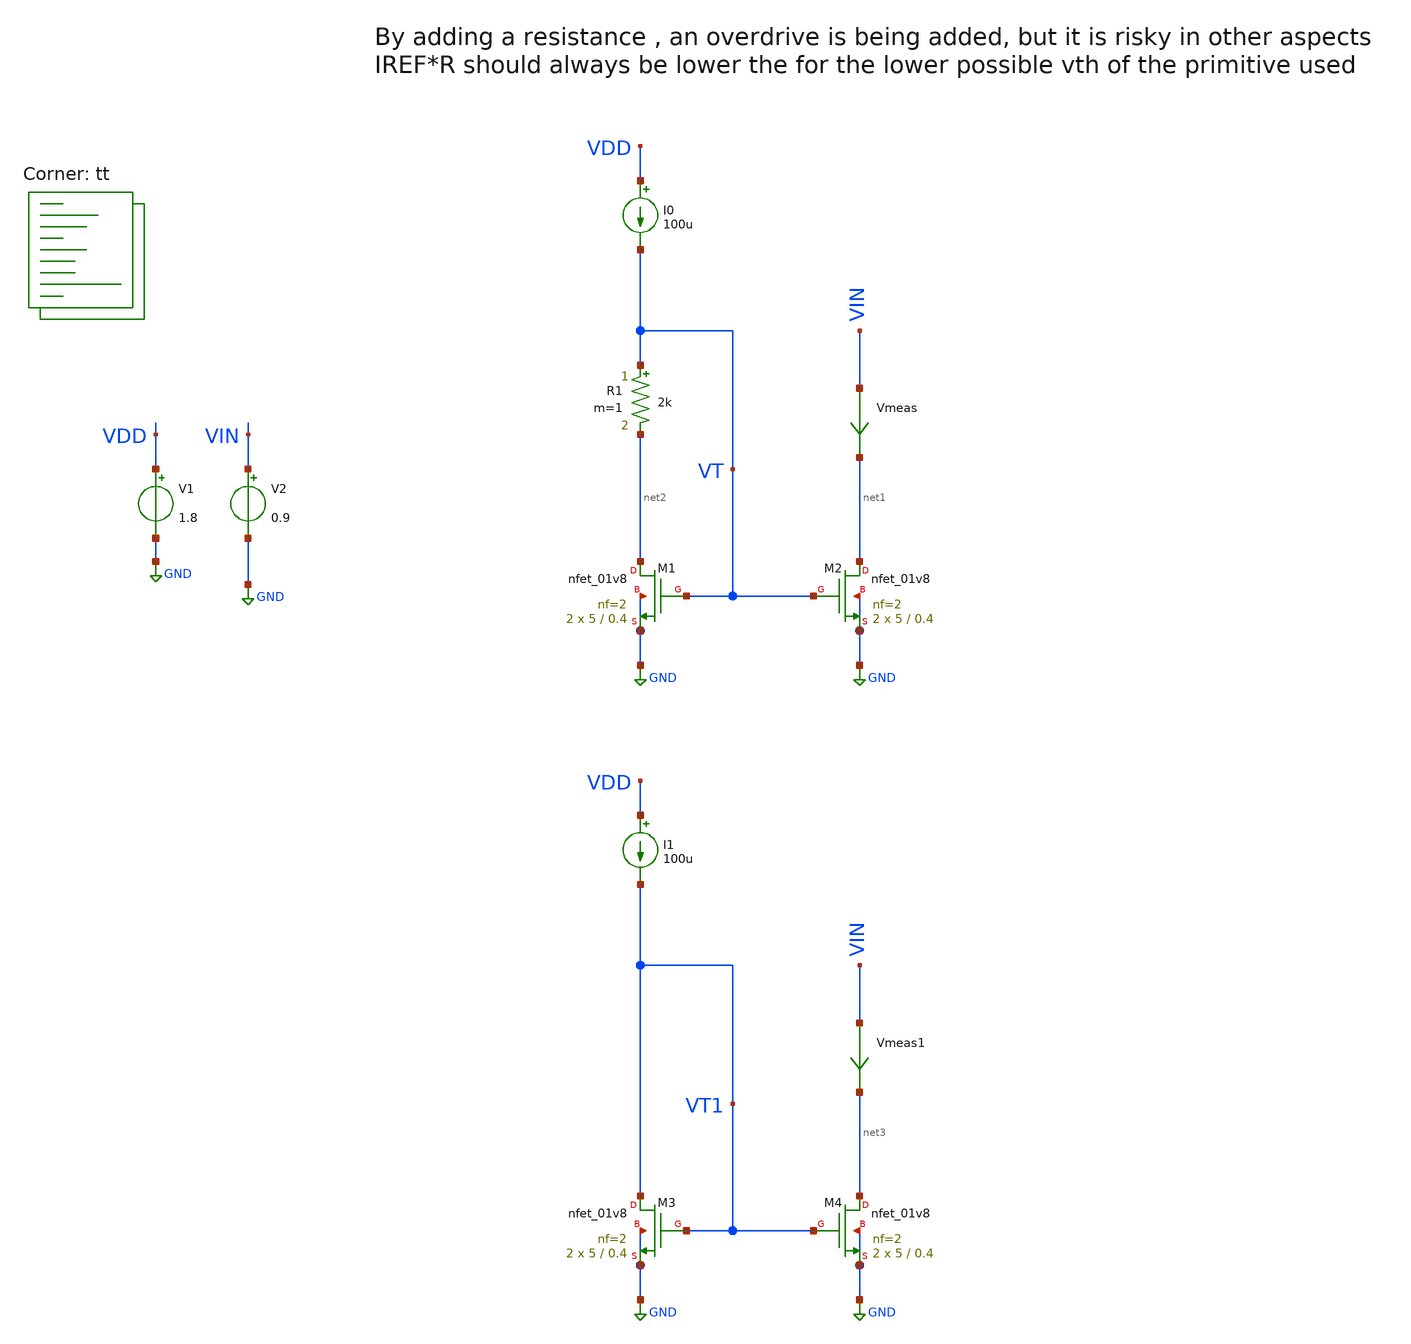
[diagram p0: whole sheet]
** sch_path: Analog_integrated_circuit_Design/chapter3/6/6.sch
**.subckt 6
V1 VDD GND 1.8
V2 VIN GND 0.9
Vmeas VIN net1 0
.save i(vmeas)
XM1 net2 VT GND GND sky130_fd_pr__nfet_01v8 L=0.4 W=5 nf=2 ad='int((2 + 1)/2) * 5 / 2 * 0.29' as='int((2 + 2)/2) * 5 / 2 * 0.29'
+ pd='2*int((2 + 1)/2) * (5 / 2 + 0.29)' ps='2*int((2 + 2)/2) * (5 / 2 + 0.29)' nrd='0.29 / 5 ' nrs='0.29 / 5 '
+ sa=0 sb=0 sd=0 mult=2 m=2
I0 VDD VT 100u
R1 VT net2 2k m=1
XM2 net1 VT GND GND sky130_fd_pr__nfet_01v8 L=0.4 W=5 nf=2 ad='int((2 + 1)/2) * 5 / 2 * 0.29' as='int((2 + 2)/2) * 5 / 2 * 0.29'
+ pd='2*int((2 + 1)/2) * (5 / 2 + 0.29)' ps='2*int((2 + 2)/2) * (5 / 2 + 0.29)' nrd='0.29 / 5 ' nrs='0.29 / 5 '
+ sa=0 sb=0 sd=0 mult=2 m=2
Vmeas1 VIN net3 0
.save i(vmeas1)
XM3 VT1 VT1 GND GND sky130_fd_pr__nfet_01v8 L=0.4 W=5 nf=2 ad='int((2 + 1)/2) * 5 / 2 * 0.29' as='int((2 + 2)/2) * 5 / 2 * 0.29'
+ pd='2*int((2 + 1)/2) * (5 / 2 + 0.29)' ps='2*int((2 + 2)/2) * (5 / 2 + 0.29)' nrd='0.29 / 5 ' nrs='0.29 / 5 '
+ sa=0 sb=0 sd=0 mult=2 m=2
I1 VDD VT1 100u
XM4 net3 VT1 GND GND sky130_fd_pr__nfet_01v8 L=0.4 W=5 nf=2 ad='int((2 + 1)/2) * 5 / 2 * 0.29' as='int((2 + 2)/2) * 5 / 2 * 0.29'
+ pd='2*int((2 + 1)/2) * (5 / 2 + 0.29)' ps='2*int((2 + 2)/2) * (5 / 2 + 0.29)' nrd='0.29 / 5 ' nrs='0.29 / 5 '
+ sa=0 sb=0 sd=0 mult=2 m=2
**** begin user architecture code
.lib $::SKYWATER_MODELS/sky130.lib.spice tt

**************************************************************
**************************************************************
**************************************************************
**************************************************************
**************************************************************
*LIBs*********************************************************
**************************************************************
**************************************************************
**************************************************************
**************************************************************
**************************************************************
*.lib $::SKYWATER_MODELS/sky130.lib.spice tt
* chose the corners in the corner file
* tt_mm for mismatch
* ss ff sf fs standart corners
* ll hh lh hl capacitor and resistors corners
* mc for total process variation including corners
**************************************************************
**************************************************************
**************************************************************
**************************************************************
**************************************************************
*Corners/montecarlo options***********************************
**************************************************************
**************************************************************
**************************************************************
**************************************************************
**************************************************************
.TEMP 27
**************************************************************
**************************************************************
**************************************************************
**************************************************************
*SIMULATION and Plots*****************************************
**************************************************************
**************************************************************
**************************************************************
**************************************************************
.control
save all
dc V2 0 1.8 0.001
*dc simulation
plot i(Vmeas) i(Vmeas1)
plot v(VT) v(VT1)
plot 1/deriv(i(Vmeas)) 1/deriv(i(Vmeas1))
.endc

**** end user architecture code
**.ends
.GLOBAL GND
.end
